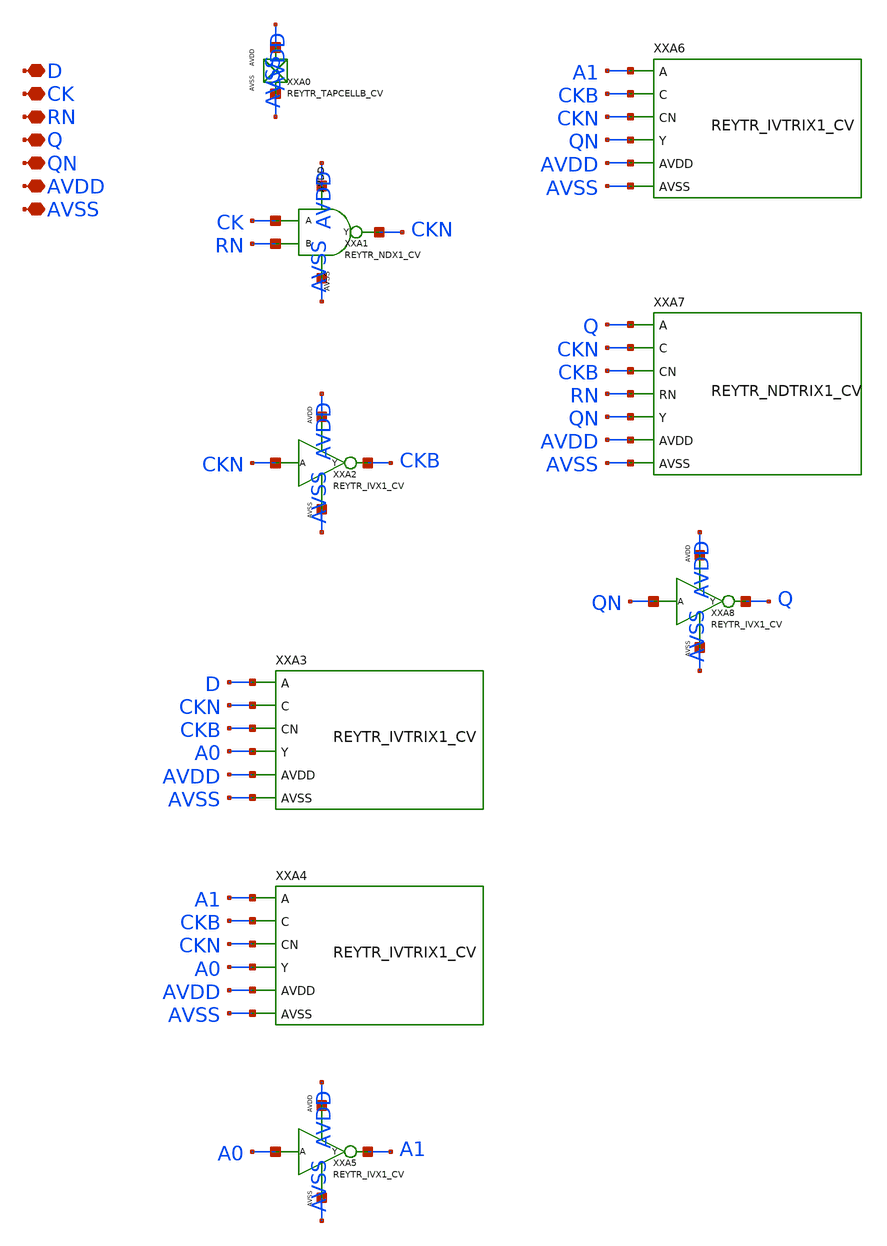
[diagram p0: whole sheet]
** sch_path: design/REY_TR_SKY130A/REYTR_DFRNQNX1_CV.sch
**.subckt REYTR_DFRNQNX1_CV D CK RN Q QN AVDD AVSS
*.iopin D
*.iopin CK
*.iopin RN
*.iopin Q
*.iopin QN
*.iopin AVDD
*.iopin AVSS
XXA0 AVDD AVSS REYTR_TAPCELLB_CV xoffset=0 yoffset=0 angle=0
XXA1 CK RN CKN AVDD AVSS REYTR_NDX1_CV
XXA2 CKN CKB AVDD AVSS REYTR_IVX1_CV
XXA3 D CKN CKB A0 AVDD AVSS REYTR_IVTRIX1_CV xoffset=0 yoffset=0 angle=0
XXA4 A1 CKB CKN A0 AVDD AVSS REYTR_IVTRIX1_CV xoffset=0 yoffset=0 angle=0
XXA5 A0 A1 AVDD AVSS REYTR_IVX1_CV
XXA6 A1 CKB CKN QN AVDD AVSS REYTR_IVTRIX1_CV xoffset=0 yoffset=0 angle=0
XXA7 Q CKN CKB RN QN AVDD AVSS REYTR_NDTRIX1_CV xoffset=0 yoffset=0 angle=0
XXA8 QN Q AVDD AVSS REYTR_IVX1_CV
**.ends
.end
